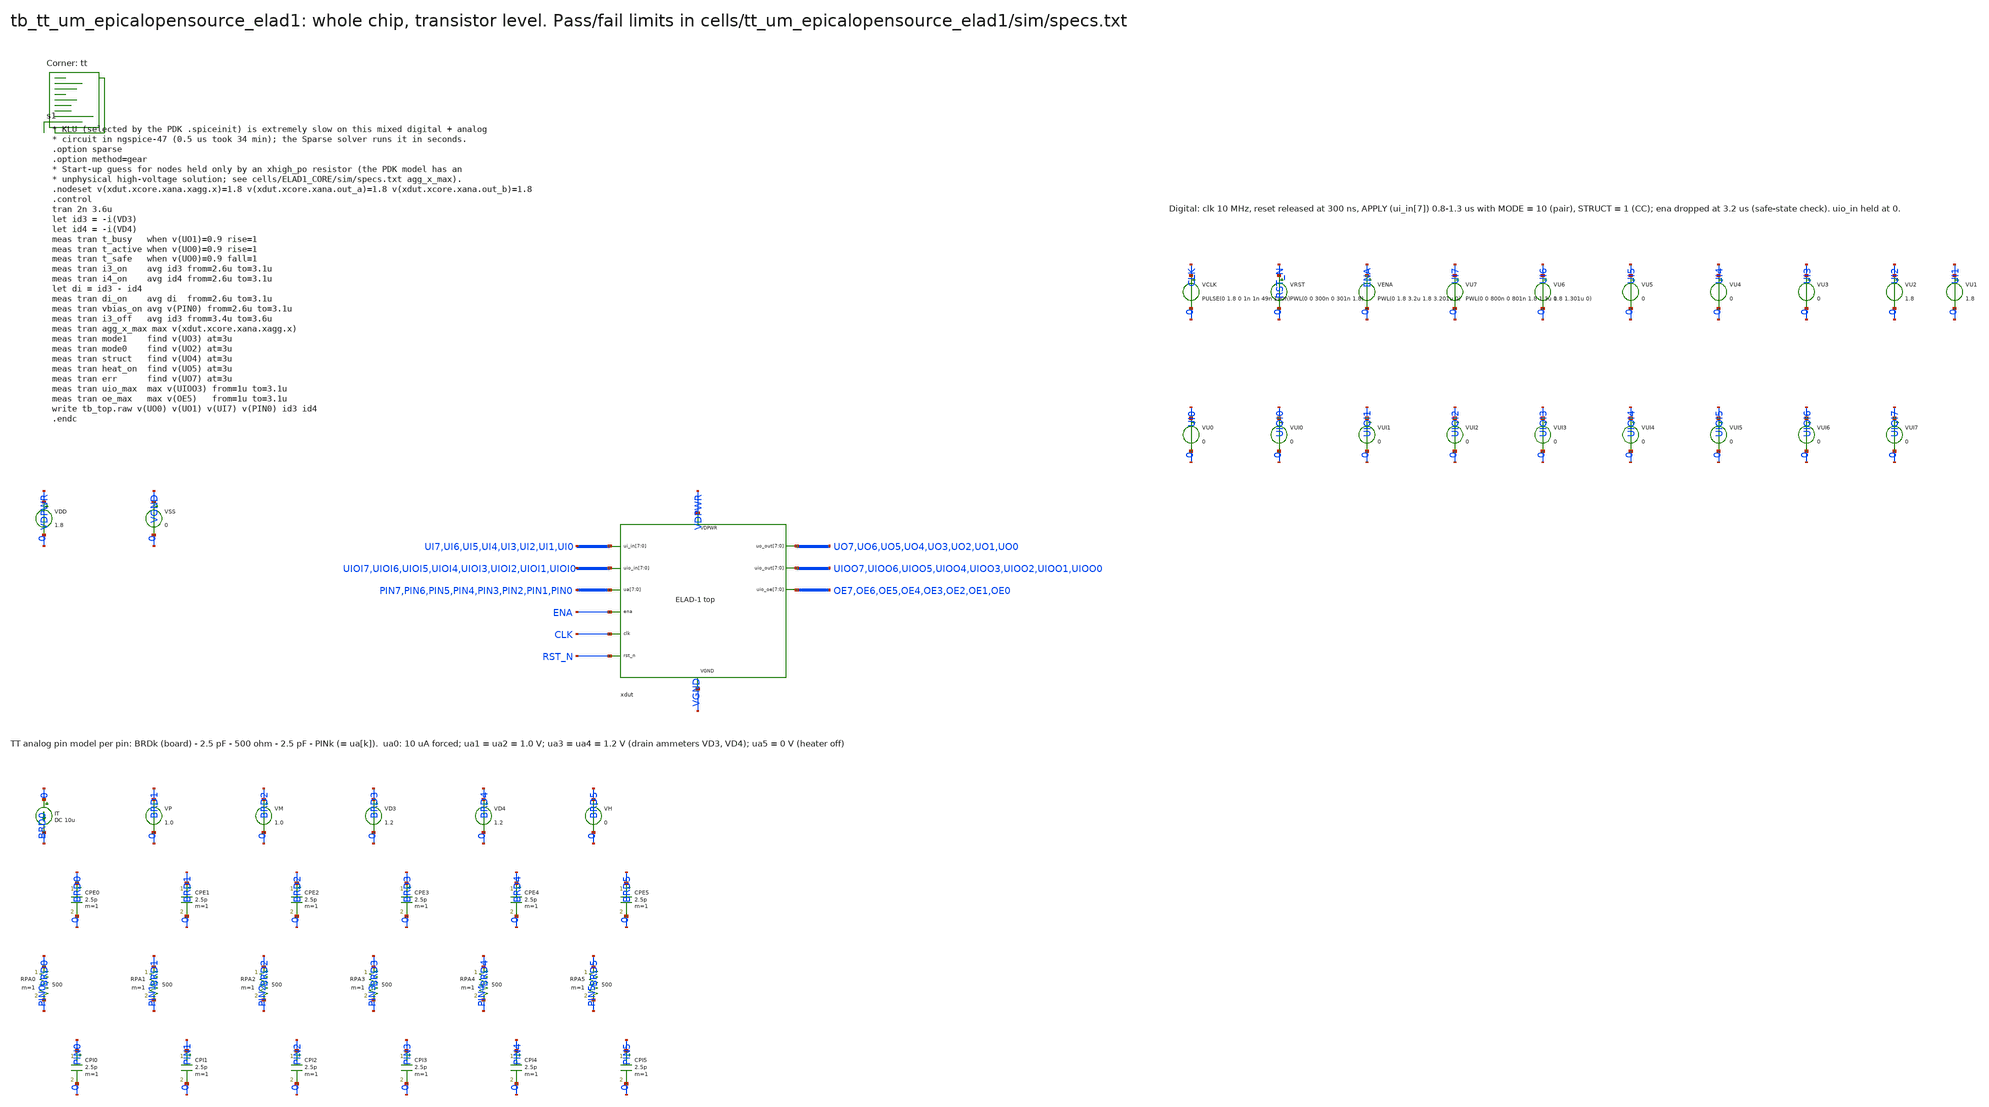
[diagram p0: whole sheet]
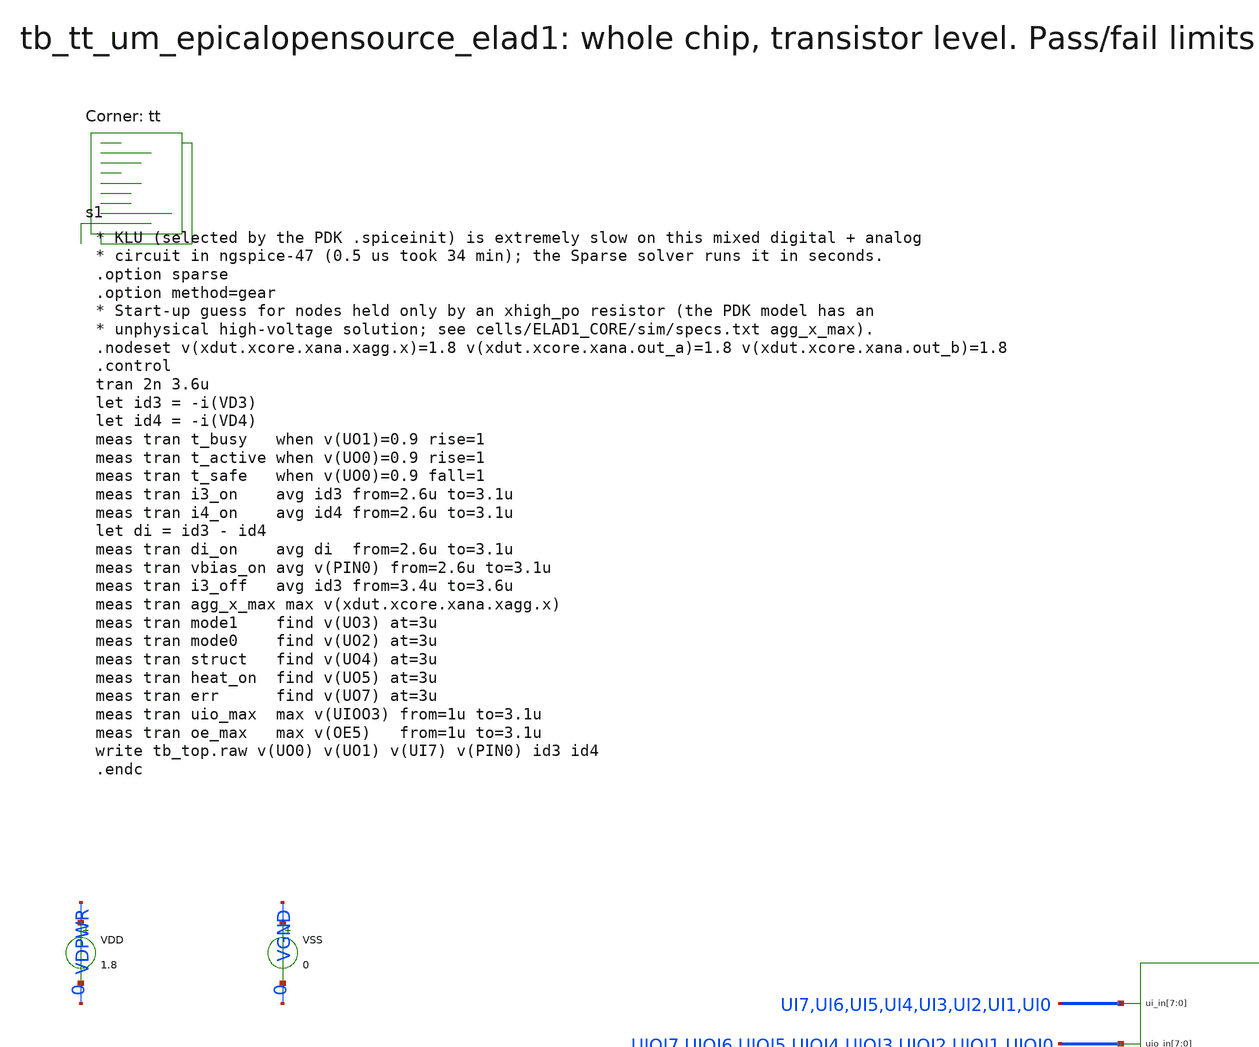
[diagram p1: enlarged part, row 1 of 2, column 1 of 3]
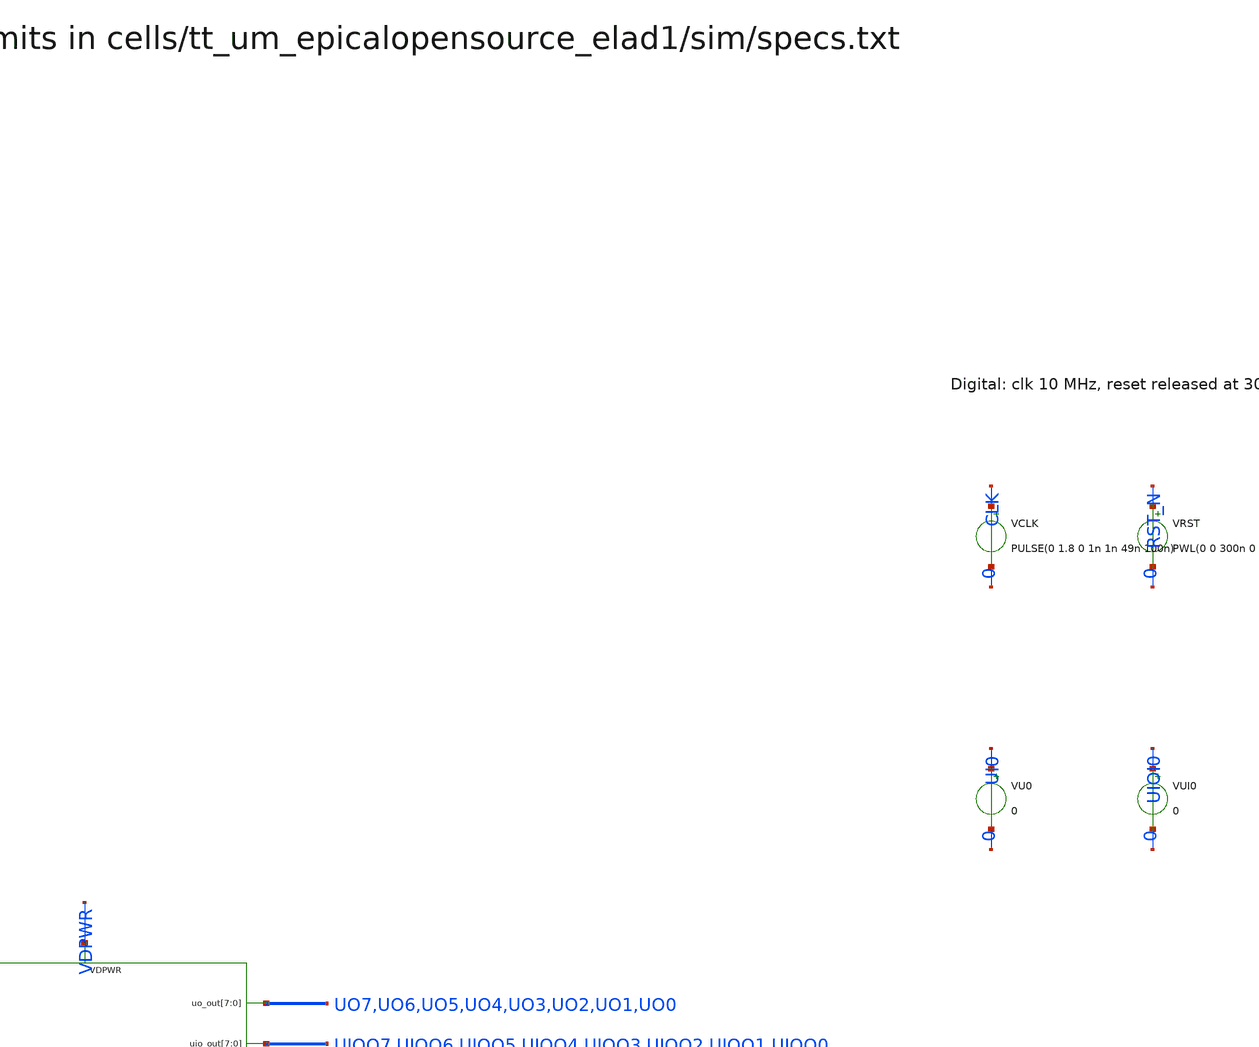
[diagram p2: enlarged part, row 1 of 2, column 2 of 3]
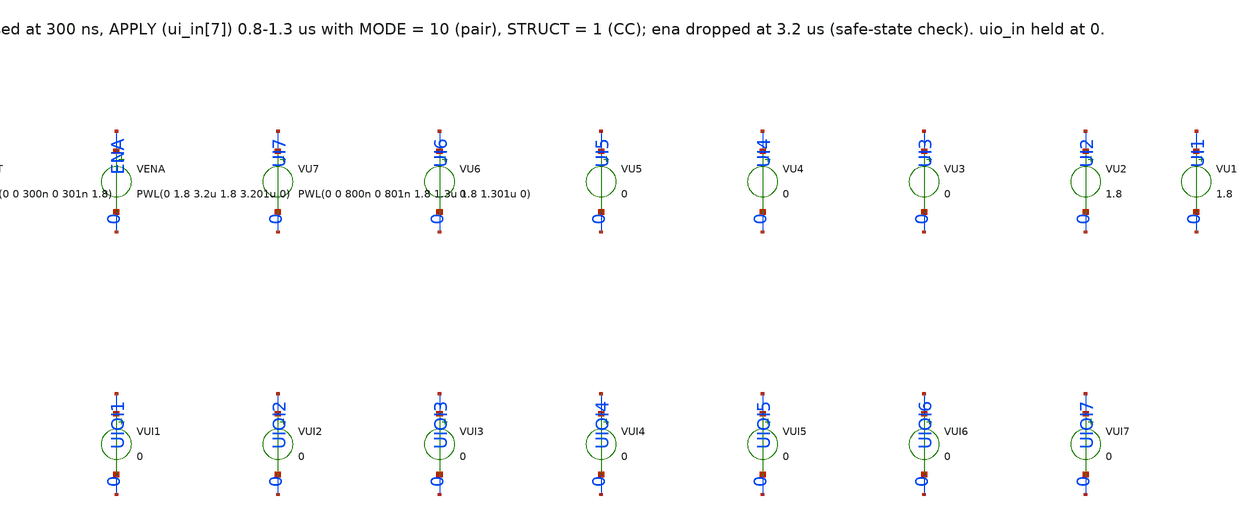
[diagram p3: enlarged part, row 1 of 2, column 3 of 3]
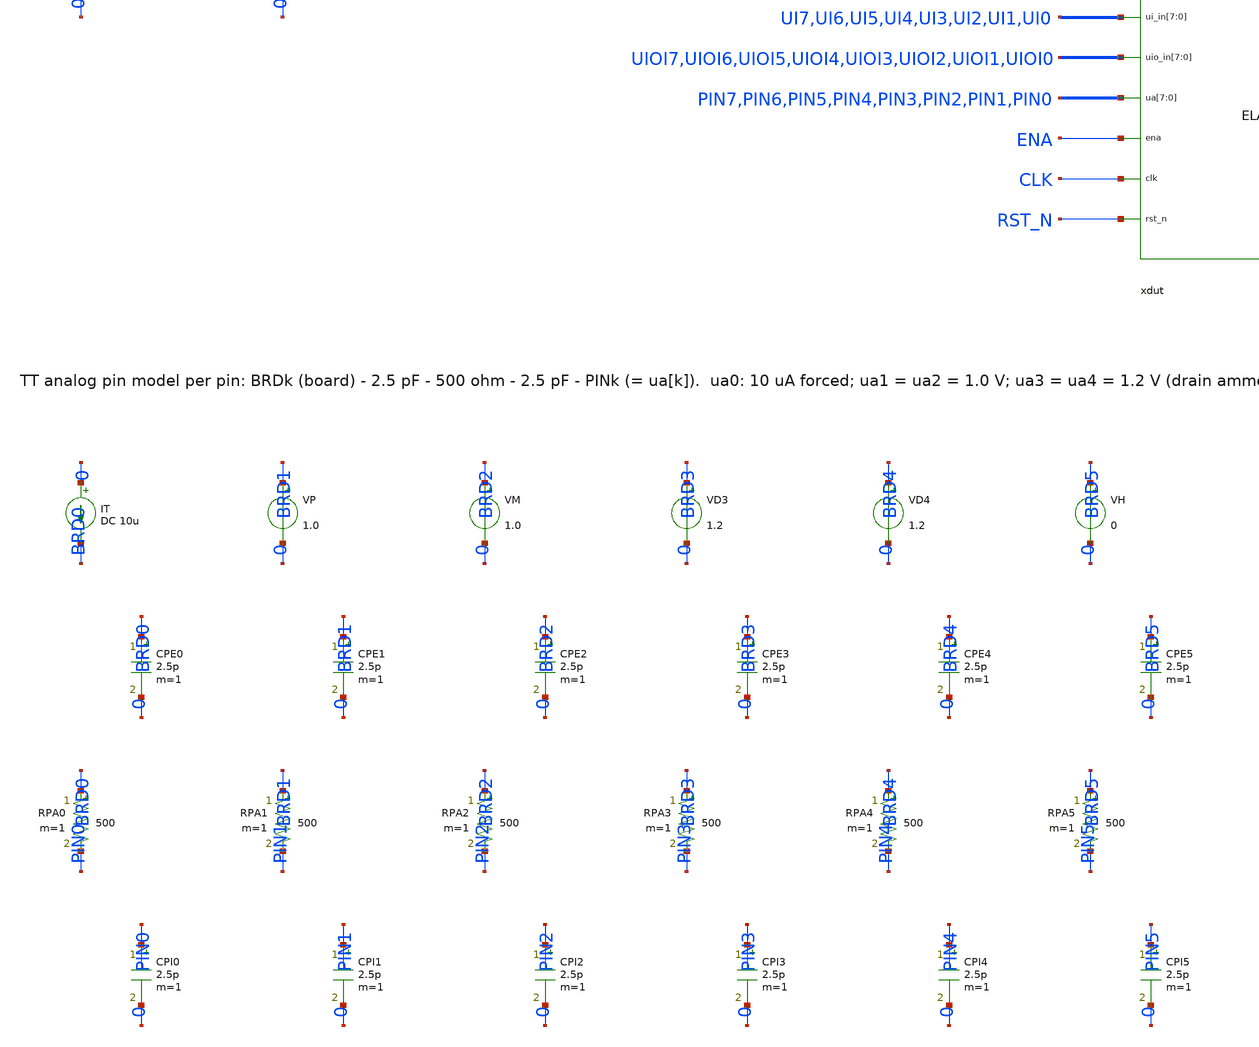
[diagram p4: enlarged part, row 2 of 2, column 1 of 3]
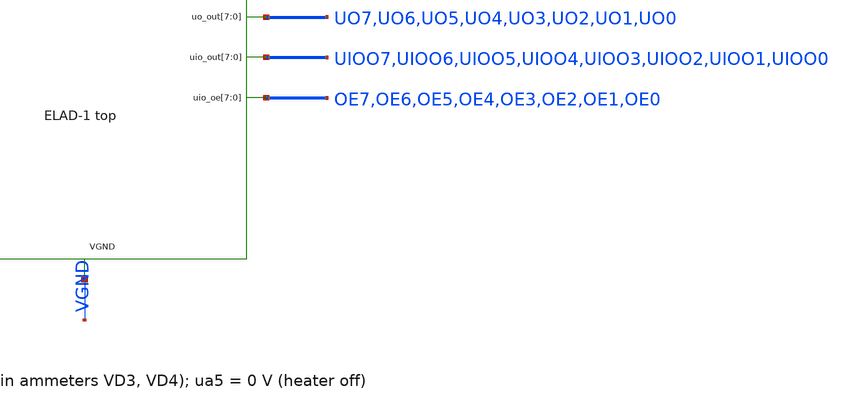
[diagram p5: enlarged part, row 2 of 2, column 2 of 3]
** sch_path: cells/tt_um_epicalopensource_elad1/schematic/tb_tt_um_epicalopensource_elad1.sch
**.subckt tb_tt_um_epicalopensource_elad1
xdut UI7 UI6 UI5 UI4 UI3 UI2 UI1 UI0 UIOI7 UIOI6 UIOI5 UIOI4 UIOI3 UIOI2 UIOI1 UIOI0 PIN7 PIN6 PIN5
+ PIN4 PIN3 PIN2 PIN1 PIN0 ENA CLK RST_N UO7 UO6 UO5 UO4 UO3 UO2 UO1 UO0 UIOO7 UIOO6 UIOO5 UIOO4 UIOO3
+ UIOO2 UIOO1 UIOO0 OE7 OE6 OE5 OE4 OE3 OE2 OE1 OE0 VDPWR VGND tt_um_epicalopensource_elad1
VDD VDPWR 0 1.8
VSS VGND 0 0
IT 0 BRD0 DC 10u
CPE0 BRD0 0 2.5p m=1
RPA0 BRD0 PIN0 500 m=1
CPI0 PIN0 0 2.5p m=1
VP BRD1 0 1.0
CPE1 BRD1 0 2.5p m=1
RPA1 BRD1 PIN1 500 m=1
CPI1 PIN1 0 2.5p m=1
VM BRD2 0 1.0
CPE2 BRD2 0 2.5p m=1
RPA2 BRD2 PIN2 500 m=1
CPI2 PIN2 0 2.5p m=1
VD3 BRD3 0 1.2
CPE3 BRD3 0 2.5p m=1
RPA3 BRD3 PIN3 500 m=1
CPI3 PIN3 0 2.5p m=1
VD4 BRD4 0 1.2
CPE4 BRD4 0 2.5p m=1
RPA4 BRD4 PIN4 500 m=1
CPI4 PIN4 0 2.5p m=1
VH BRD5 0 0
CPE5 BRD5 0 2.5p m=1
RPA5 BRD5 PIN5 500 m=1
CPI5 PIN5 0 2.5p m=1
VCLK CLK 0 PULSE(0 1.8 0 1n 1n 49n 100n)
VRST RST_N 0 PWL(0 0 300n 0 301n 1.8)
VENA ENA 0 PWL(0 1.8 3.2u 1.8 3.201u 0)
VU7 UI7 0 PWL(0 0 800n 0 801n 1.8 1.3u 1.8 1.301u 0)
VU6 UI6 0 0
VU5 UI5 0 0
VU4 UI4 0 0
VU3 UI3 0 0
VU2 UI2 0 1.8
VU1 UI1 0 1.8
VU0 UI0 0 0
VUI0 UIOI0 0 0
VUI1 UIOI1 0 0
VUI2 UIOI2 0 0
VUI3 UIOI3 0 0
VUI4 UIOI4 0 0
VUI5 UIOI5 0 0
VUI6 UIOI6 0 0
VUI7 UIOI7 0 0
**** begin user architecture code
.lib $::SKYWATER_MODELS/sky130.lib.spice tt

* KLU (selected by the PDK .spiceinit) is extremely slow on this mixed digital + analog
* circuit in ngspice-47 (0.5 us took 34 min); the Sparse solver runs it in seconds.
.option sparse
.option method=gear
* Start-up guess for nodes held only by an xhigh_po resistor (the PDK model has an
* unphysical high-voltage solution; see cells/ELAD1_CORE/sim/specs.txt agg_x_max).
.nodeset v(xdut.xcore.xana.xagg.x)=1.8 v(xdut.xcore.xana.out_a)=1.8 v(xdut.xcore.xana.out_b)=1.8
.control
tran 2n 3.6u
let id3 = -i(VD3)
let id4 = -i(VD4)
meas tran t_busy   when v(UO1)=0.9 rise=1
meas tran t_active when v(UO0)=0.9 rise=1
meas tran t_safe   when v(UO0)=0.9 fall=1
meas tran i3_on    avg id3 from=2.6u to=3.1u
meas tran i4_on    avg id4 from=2.6u to=3.1u
let di = id3 - id4
meas tran di_on    avg di  from=2.6u to=3.1u
meas tran vbias_on avg v(PIN0) from=2.6u to=3.1u
meas tran i3_off   avg id3 from=3.4u to=3.6u
meas tran agg_x_max max v(xdut.xcore.xana.xagg.x)
meas tran mode1    find v(UO3) at=3u
meas tran mode0    find v(UO2) at=3u
meas tran struct   find v(UO4) at=3u
meas tran heat_on  find v(UO5) at=3u
meas tran err      find v(UO7) at=3u
meas tran uio_max  max v(UIOO3) from=1u to=3.1u
meas tran oe_max   max v(OE5)   from=1u to=3.1u
write tb_top.raw v(UO0) v(UO1) v(UI7) v(PIN0) id3 id4
.endc

**** end user architecture code
**.ends
.end
